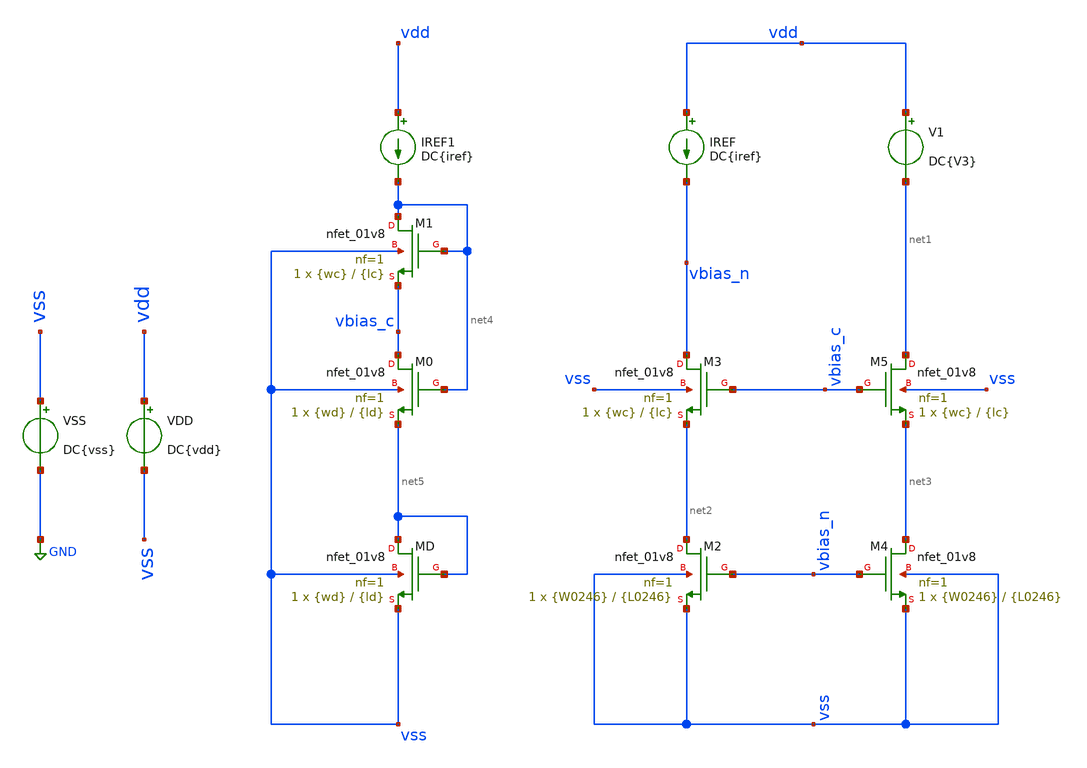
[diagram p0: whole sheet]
** sch_path: TP2/tp2_3b.sch
**.subckt tp2_3b
XM2 net2 vbias_n vss vss sky130_fd_pr__nfet_01v8 L={L0246} W={W0246} nf=1 ad='int((nf+1)/2) * W/nf * 0.29'
+ as='int((nf+2)/2) * W/nf * 0.29' pd='2*int((nf+1)/2) * (W/nf + 0.29)' ps='2*int((nf+2)/2) * (W/nf + 0.29)'
+ nrd='0.29 / W' nrs='0.29 / W' sa=0 sb=0 sd=0 mult=1 m=1
XM4 net3 vbias_n vss vss sky130_fd_pr__nfet_01v8 L={L0246} W={W0246} nf=1 ad='int((nf+1)/2) * W/nf * 0.29'
+ as='int((nf+2)/2) * W/nf * 0.29' pd='2*int((nf+1)/2) * (W/nf + 0.29)' ps='2*int((nf+2)/2) * (W/nf + 0.29)'
+ nrd='0.29 / W' nrs='0.29 / W' sa=0 sb=0 sd=0 mult=1 m=1
IREF vdd vbias_n DC{iref}
VSS vss GND DC{vss}
VDD vdd vss DC{vdd}
XM5 net1 vbias_c net3 vss sky130_fd_pr__nfet_01v8 L={lc} W={wc} nf=1 ad='int((nf+1)/2) * W/nf * 0.29'
+ as='int((nf+2)/2) * W/nf * 0.29' pd='2*int((nf+1)/2) * (W/nf + 0.29)' ps='2*int((nf+2)/2) * (W/nf + 0.29)'
+ nrd='0.29 / W' nrs='0.29 / W' sa=0 sb=0 sd=0 mult=1 m=1
V1 vdd net1 DC{V3}
XM3 vbias_n vbias_c net2 vss sky130_fd_pr__nfet_01v8 L={lc} W={wc} nf=1 ad='int((nf+1)/2) * W/nf * 0.29'
+ as='int((nf+2)/2) * W/nf * 0.29' pd='2*int((nf+1)/2) * (W/nf + 0.29)' ps='2*int((nf+2)/2) * (W/nf + 0.29)'
+ nrd='0.29 / W' nrs='0.29 / W' sa=0 sb=0 sd=0 mult=1 m=1
IREF1 vdd net4 DC{iref}
XM1 net4 net4 vbias_c vss sky130_fd_pr__nfet_01v8 L={lc} W={wc} nf=1 ad='int((nf+1)/2) * W/nf * 0.29'
+ as='int((nf+2)/2) * W/nf * 0.29' pd='2*int((nf+1)/2) * (W/nf + 0.29)' ps='2*int((nf+2)/2) * (W/nf + 0.29)'
+ nrd='0.29 / W' nrs='0.29 / W' sa=0 sb=0 sd=0 mult=1 m=1
XM0 vbias_c net4 net5 vss sky130_fd_pr__nfet_01v8 L={ld} W={wd} nf=1 ad='int((nf+1)/2) * W/nf * 0.29'
+ as='int((nf+2)/2) * W/nf * 0.29' pd='2*int((nf+1)/2) * (W/nf + 0.29)' ps='2*int((nf+2)/2) * (W/nf + 0.29)'
+ nrd='0.29 / W' nrs='0.29 / W' sa=0 sb=0 sd=0 mult=1 m=1
XMD net5 net5 vss vss sky130_fd_pr__nfet_01v8 L={ld} W={wd} nf=1 ad='int((nf+1)/2) * W/nf * 0.29' as='int((nf+2)/2) * W/nf * 0.29'
+ pd='2*int((nf+1)/2) * (W/nf + 0.29)' ps='2*int((nf+2)/2) * (W/nf + 0.29)' nrd='0.29 / W' nrs='0.29 / W'
+ sa=0 sb=0 sd=0 mult=1 m=1
**** begin user architecture code



* Parameters
.param vdd = 1.8
.param vss = 0.0
.param V3 = 1.2
.param iref = 200u
.param L0246 = 0.15
.param lc = 0.9
.param ld = 0.9
.param W0246 = 5
.param wc = 70
.param wd = 20
.options TEMPS = 27.0

* Models
.lib ~/skywater/skywater-pdk/libraries/sky130_fd_pr_ngspice/latest/models/corners/sky130.lib TT

* Data to save
.save all  @M.XM0.msky130_fd_pr__nfet_01v8[id]  @M.XM0.msky130_fd_pr__nfet_01v8[gm]  @M.XM0.msky130_fd_pr__nfet_01v8[vds]  @M.XM0.msky130_fd_pr__nfet_01v8[vgs]  @M.XM0.msky130_fd_pr__nfet_01v8[w]  @M.XM0.msky130_fd_pr__nfet_01v8[vth]  @M.XM0.msky130_fd_pr__nfet_01v8[vdsat]  @M.XM1.msky130_fd_pr__nfet_01v8[id]  @M.XM1.msky130_fd_pr__nfet_01v8[gm]  @M.XM1.msky130_fd_pr__nfet_01v8[vds]  @M.XM1.msky130_fd_pr__nfet_01v8[vgs]  @M.XM1.msky130_fd_pr__nfet_01v8[w]  @M.XM1.msky130_fd_pr__nfet_01v8[vth]  @M.XM1.msky130_fd_pr__nfet_01v8[vdsat]  @M.XM2.msky130_fd_pr__nfet_01v8[id]  @M.XM2.msky130_fd_pr__nfet_01v8[gm]  @M.XM2.msky130_fd_pr__nfet_01v8[vds]  @M.XM2.msky130_fd_pr__nfet_01v8[vgs]  @M.XM2.msky130_fd_pr__nfet_01v8[w]  @M.XM2.msky130_fd_pr__nfet_01v8[vth]  @M.XM2.msky130_fd_pr__nfet_01v8[vdsat]  @M.XM3.msky130_fd_pr__nfet_01v8[id]  @M.XM3.msky130_fd_pr__nfet_01v8[gm]  @M.XM3.msky130_fd_pr__nfet_01v8[vds]  @M.XM3.msky130_fd_pr__nfet_01v8[vgs]  @M.XM3.msky130_fd_pr__nfet_01v8[w]  @M.XM3.msky130_fd_pr__nfet_01v8[vth]  @M.XM3.msky130_fd_pr__nfet_01v8[vdsat]  @M.XM4.msky130_fd_pr__nfet_01v8[id]  @M.XM4.msky130_fd_pr__nfet_01v8[gm]  @M.XM4.msky130_fd_pr__nfet_01v8[vds]  @M.XM4.msky130_fd_pr__nfet_01v8[vgs]  @M.XM4.msky130_fd_pr__nfet_01v8[w]  @M.XM4.msky130_fd_pr__nfet_01v8[vth]  @M.XM4.msky130_fd_pr__nfet_01v8[vdsat]  @M.XM5.msky130_fd_pr__nfet_01v8[id]  @M.XM5.msky130_fd_pr__nfet_01v8[gm]  @M.XM5.msky130_fd_pr__nfet_01v8[vds]  @M.XM5.msky130_fd_pr__nfet_01v8[vgs]  @M.XM5.msky130_fd_pr__nfet_01v8[w]  @M.XM5.msky130_fd_pr__nfet_01v8[vth]  @M.XM5.msky130_fd_pr__nfet_01v8[vdsat]  @M.XMD.msky130_fd_pr__nfet_01v8[id]  @M.XMD.msky130_fd_pr__nfet_01v8[gm]  @M.XMD.msky130_fd_pr__nfet_01v8[vds]  @M.XMD.msky130_fd_pr__nfet_01v8[vgs]  @M.XMD.msky130_fd_pr__nfet_01v8[w]  @M.XMD.msky130_fd_pr__nfet_01v8[vth]  @M.XMD.msky130_fd_pr__nfet_01v8[vdsat]


* Simulation
.control
  op
  save all
  unset filetype
  write tp2_3b.raw

.endc

.end


**** end user architecture code
**.ends
.GLOBAL GND
.end
